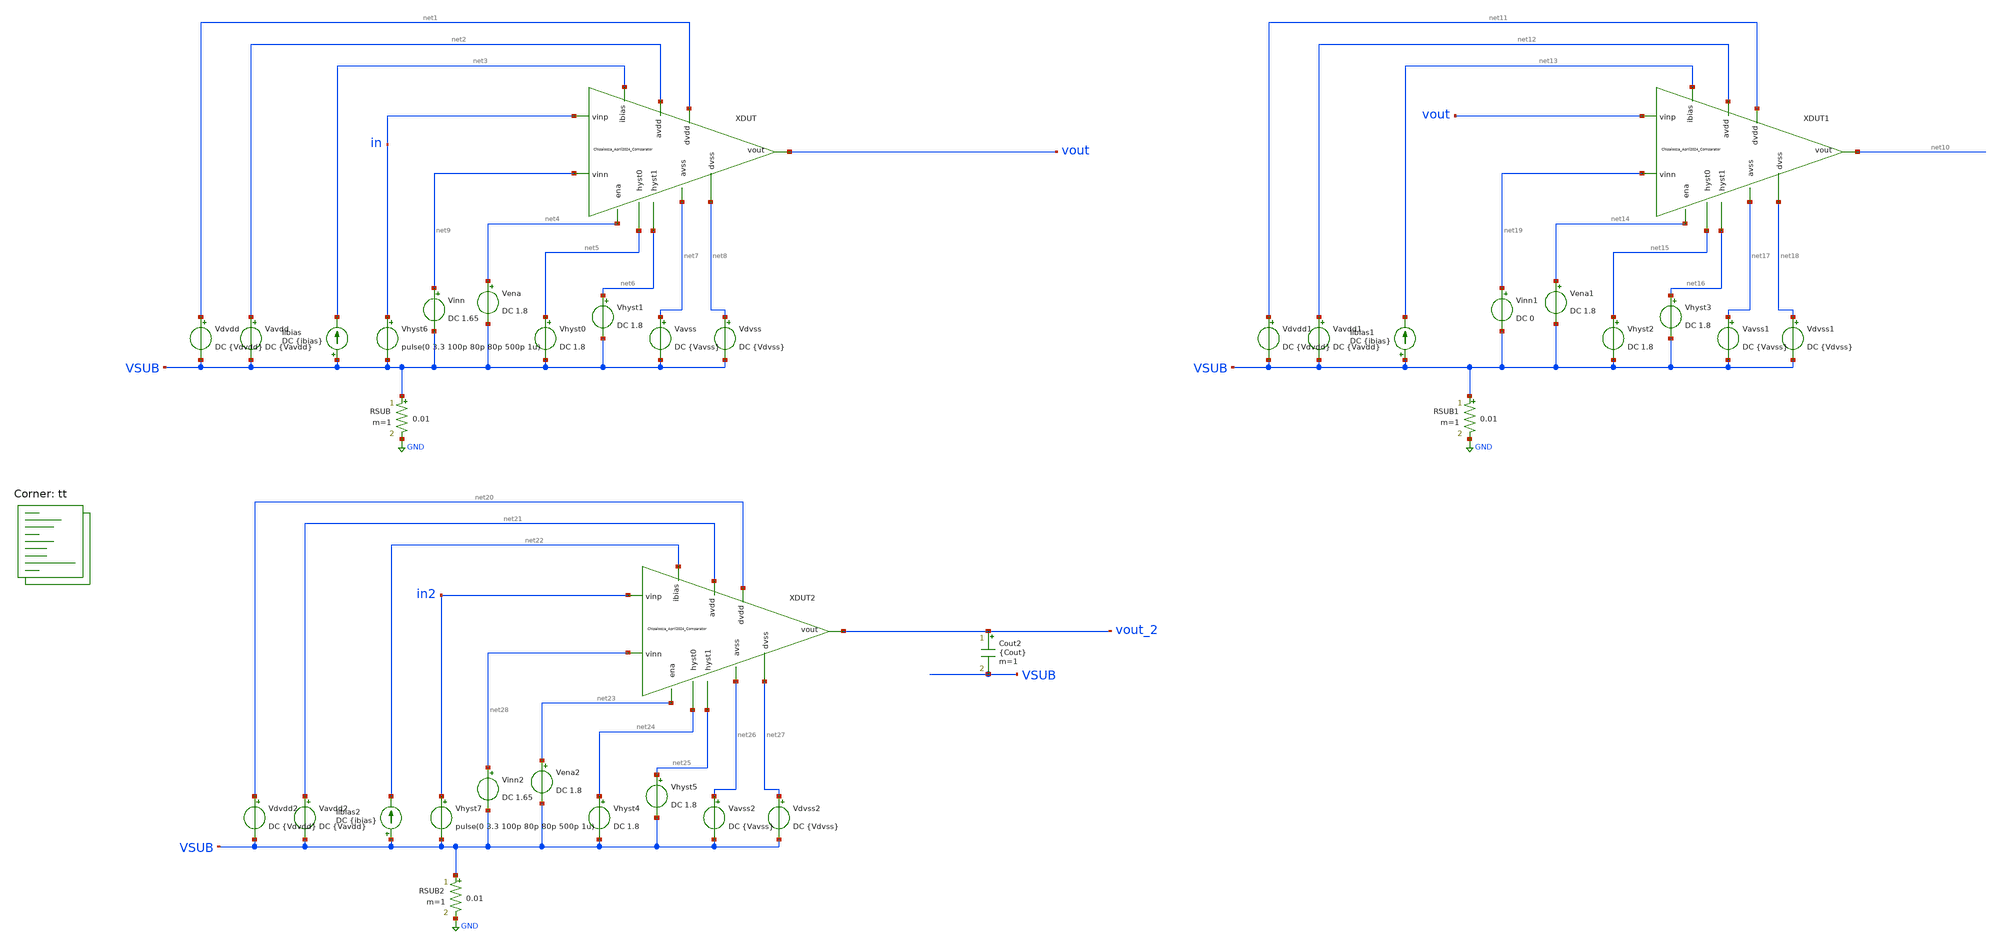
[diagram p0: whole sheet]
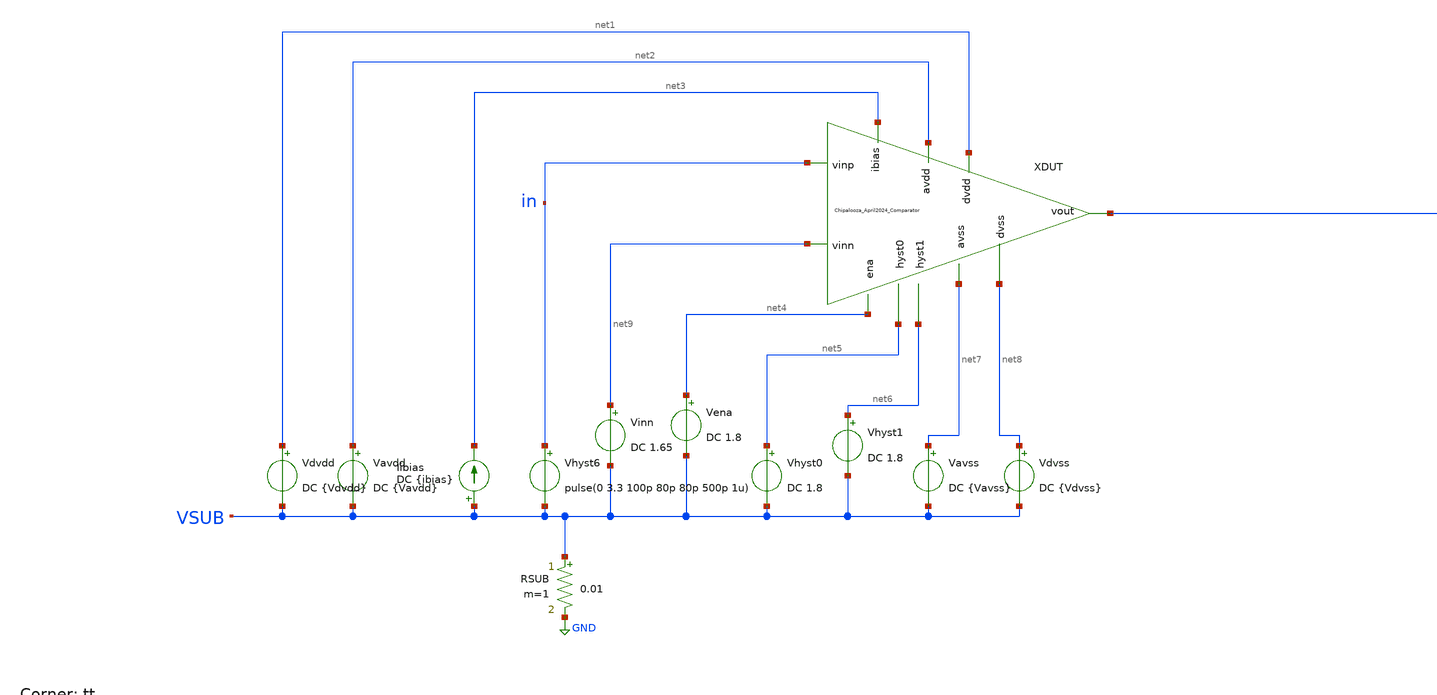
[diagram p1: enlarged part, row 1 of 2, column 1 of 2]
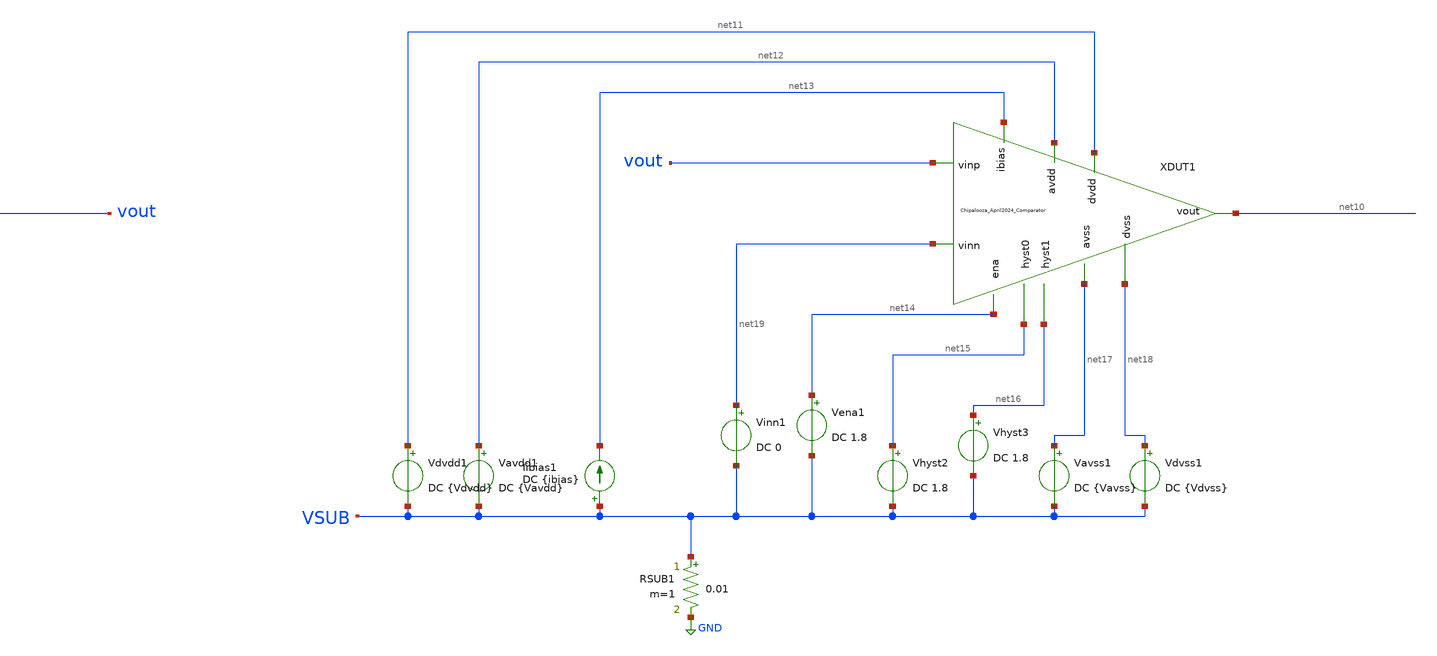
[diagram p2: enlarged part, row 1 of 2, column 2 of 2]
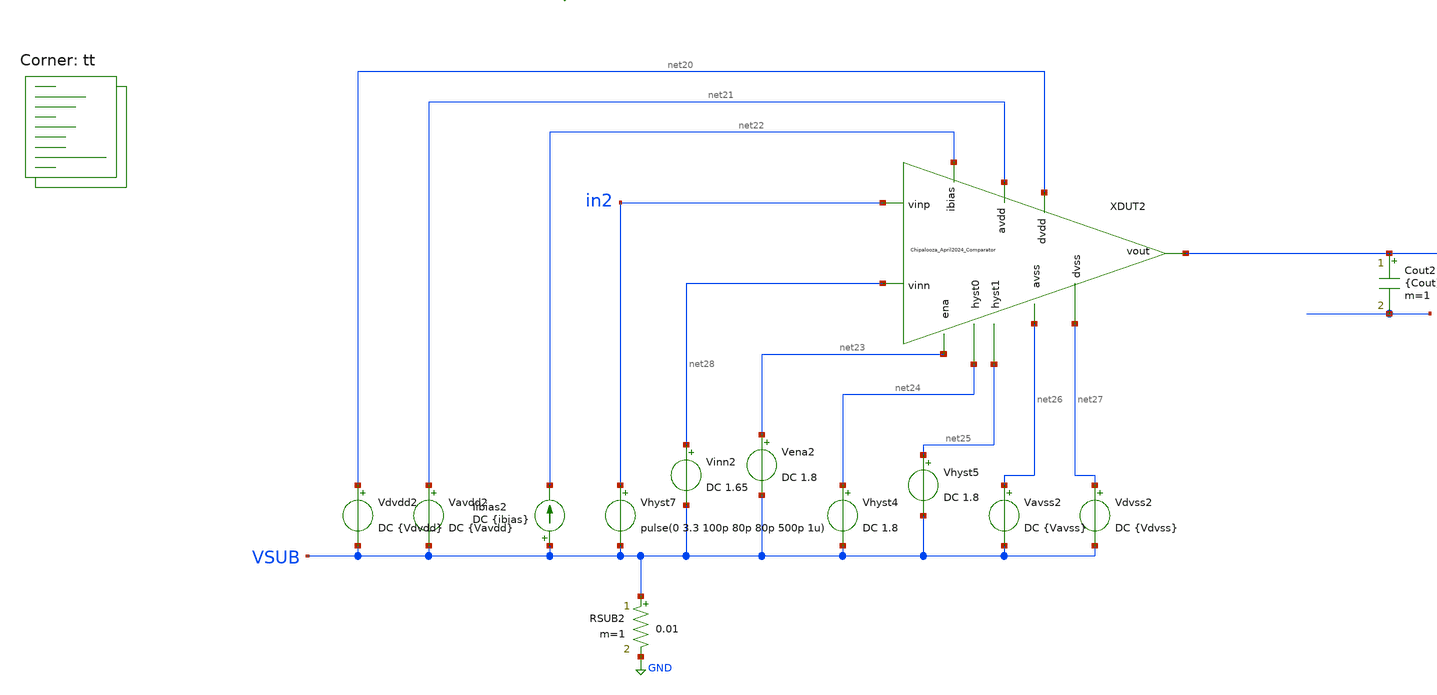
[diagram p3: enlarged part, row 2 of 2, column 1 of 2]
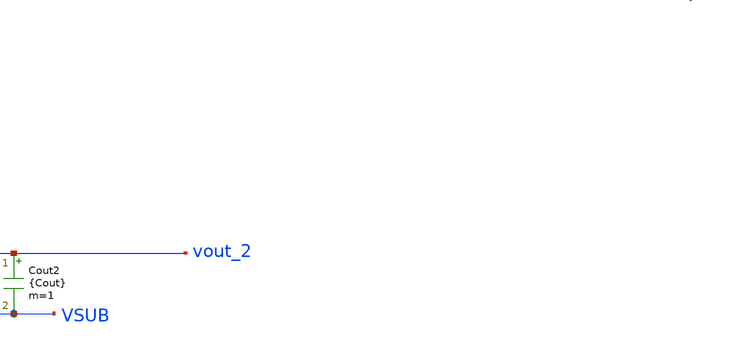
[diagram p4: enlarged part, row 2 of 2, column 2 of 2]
** sch_path: Chipalooza_April2024_Comparator/xschem/TB_inputCapacitance.sch
**.subckt TB_inputCapacitance
Vavdd net2 VSUB DC {Vavdd}
Vdvdd net1 VSUB DC {Vdvdd}
Vena net4 VSUB DC 1.8
Vhyst0 net5 VSUB DC 1.8
Vhyst1 net6 VSUB DC 1.8
Vavss net7 VSUB DC {Vavss}
Vdvss net8 VSUB DC {Vdvss}
RSUB VSUB GND 0.01 m=1
Iibias VSUB net3 DC {ibias}
XDUT net5 net6 net2 in net7 net9 net1 net8 vout net3 net4 Chipalooza_April2024_Comparator
Vinn net9 VSUB DC 1.65
Vavdd1 net12 VSUB DC {Vavdd}
Vdvdd1 net11 VSUB DC {Vdvdd}
Vena1 net14 VSUB DC 1.8
Vhyst2 net15 VSUB DC 1.8
Vhyst3 net16 VSUB DC 1.8
Vavss1 net17 VSUB DC {Vavss}
Vdvss1 net18 VSUB DC {Vdvss}
RSUB1 VSUB GND 0.01 m=1
Iibias1 VSUB net13 DC {ibias}
XDUT1 net15 net16 net12 vout net17 net19 net11 net18 net10 net13 net14
+ Chipalooza_April2024_Comparator
Vavdd2 net21 VSUB DC {Vavdd}
Cout2 vout_2 VSUB {Cout} m=1
Vdvdd2 net20 VSUB DC {Vdvdd}
Vena2 net23 VSUB DC 1.8
Vhyst4 net24 VSUB DC 1.8
Vhyst5 net25 VSUB DC 1.8
Vavss2 net26 VSUB DC {Vavss}
Vdvss2 net27 VSUB DC {Vdvss}
RSUB2 VSUB GND 0.01 m=1
Iibias2 VSUB net22 DC {ibias}
XDUT2 net24 net25 net21 in2 net26 net28 net20 net27 vout_2 net22 net23
+ Chipalooza_April2024_Comparator
Vinn2 net28 VSUB DC 1.65
Vhyst6 in VSUB pulse(0 3.3 100p 80p 80p 500p 1u)
Vhyst7 in2 VSUB pulse(0 3.3 100p 80p 80p 500p 1u)
Vinn1 net19 VSUB DC 0
**** begin user architecture code
.lib $::SKYWATER_MODELS/sky130.lib.spice tt

* this option enables mos model bin
* selection based on W/NF instead of W
*.option wnflag=1
.option savecurrents
.option save all

.control

.param vdvdd=1.8 vavdd=3.3
.param ibias=1u ena=1 Vhyst_0=1 Vhyst_1=1
.param vavss=0 vdvss=0
.param Vcm=1.65
.parm vd=3.3

.param cout=1pF

tran 1ps 1ns
plot v(vout) v(vout_2)


* Measure rising and falling edge (with respect to the output edge) time delays for
* the real copy of the circuit.
*meas TRAN tdr   TRIG v(in) VAL='0.5*vd' FALL=1 TARG v(vout) VAL='0.5*vd' RISE=1
*meas TRAN tdf   TRIG v(in) VAL='0.5*vd' RISE=1 TARG v(vout) VAL='0.5*vd' FALL=1
*meas TRAN tdavg PARAM='(tdr+tdf)/2'

* Measure the same parameters for the model circuit loaded by CLOAD
*meas TRAN tdrc   TRIG v(in2) VAL='0.5*vd' FALL=1 TARG v(vout2) VAL='0.5*vd' RISE=1
*meas TRAN tdfc   TRIG v(in2) VAL='0.5*vd' RISE=1 TARG v(vout2) VAL='0.5*vd' FALL=1
*meas TRAN tdavgc PARAM='(tdrc+tdfc)/2' GOAL=tdavg

*print tdr tdf tdavg tdrc tdfc tdavgc

write TB_inputCapacitance.raw


*quit 0

.endc


**** end user architecture code
**.ends

* expanding   symbol:  Chipalooza_April2024_Comparator.sym # of pins=11
** sym_path: Chipalooza_April2024_Comparator/xschem/Chipalooza_April2024_Comparator.sym
** sch_path: Chipalooza_April2024_Comparator/xschem/Chipalooza_April2024_Comparator.sch
.subckt Chipalooza_April2024_Comparator hyst0 hyst1 avdd vinp avss vinn dvdd dvss vout ibias ena
*.ipin vinp
*.ipin vinn
*.ipin hyst0
*.ipin hyst1
*.ipin avdd
*.ipin avss
*.ipin dvdd
*.ipin dvss
*.opin vout
*.ipin ena
*.ipin ibias
XM29 SumOutBar SumOut dvdd dvdd sky130_fd_pr__pfet_01v8 L=1 W=2 nf=1 ad='int((nf+1)/2) * W/nf * 0.29'
+ as='int((nf+2)/2) * W/nf * 0.29' pd='2*int((nf+1)/2) * (W/nf + 0.29)' ps='2*int((nf+2)/2) * (W/nf + 0.29)'
+ nrd='0.29 / W' nrs='0.29 / W' sa=0 sb=0 sd=0 mult=2 m=2
XM30 SumOutBar SumOut dvssi dvss sky130_fd_pr__nfet_01v8 L=1 W=2 nf=1 ad='int((nf+1)/2) * W/nf * 0.29'
+ as='int((nf+2)/2) * W/nf * 0.29' pd='2*int((nf+1)/2) * (W/nf + 0.29)' ps='2*int((nf+2)/2) * (W/nf + 0.29)'
+ nrd='0.29 / W' nrs='0.29 / W' sa=0 sb=0 sd=0 mult=2 m=2
XM25 net2 hyst_bias0 avss avss sky130_fd_pr__nfet_g5v0d10v5 L=1 W=3 nf=1 ad='int((nf+1)/2) * W/nf * 0.29'
+ as='int((nf+2)/2) * W/nf * 0.29' pd='2*int((nf+1)/2) * (W/nf + 0.29)' ps='2*int((nf+2)/2) * (W/nf + 0.29)'
+ nrd='0.29 / W' nrs='0.29 / W' sa=0 sb=0 sd=0 mult=2 m=2
XM26 hyst_bias0 ibias dvssi dvss sky130_fd_pr__nfet_01v8 L=1 W=3 nf=1 ad='int((1 + 1)/2) * 3 / 1 * 0.29'
+ as='int((1 + 2)/2) * 3 / 1 * 0.29' pd='2*int((1 + 1)/2) * (3 / 1 + 0.29)' ps='2*int((1 + 2)/2) * (3 / 1 + 0.29)'
+ nrd='0.29 / 3 ' nrs='0.29 / 3 ' sa=0 sb=0 sd=0 mult=2 m=2
XM27 ibias ibias dvssi dvss sky130_fd_pr__nfet_01v8 L=1 W=3 nf=1 ad='int((1 + 1)/2) * 3 / 1 * 0.29' as='int((1 + 2)/2) * 3 / 1 * 0.29'
+ pd='2*int((1 + 1)/2) * (3 / 1 + 0.29)' ps='2*int((1 + 2)/2) * (3 / 1 + 0.29)' nrd='0.29 / 3 ' nrs='0.29 / 3 '
+ sa=0 sb=0 sd=0 mult=2 m=2
XM34 hyst_bias1 hyst_bias0 dvdd dvdd sky130_fd_pr__pfet_01v8 L=1 W=3 nf=1 ad='int((nf+1)/2) * W/nf * 0.29'
+ as='int((nf+2)/2) * W/nf * 0.29' pd='2*int((nf+1)/2) * (W/nf + 0.29)' ps='2*int((nf+2)/2) * (W/nf + 0.29)'
+ nrd='0.29 / W' nrs='0.29 / W' sa=0 sb=0 sd=0 mult=2 m=2
XM35 hyst_bias0 hyst_bias0 dvdd dvdd sky130_fd_pr__pfet_01v8 L=1 W=3 nf=1 ad='int((nf+1)/2) * W/nf * 0.29'
+ as='int((nf+2)/2) * W/nf * 0.29' pd='2*int((nf+1)/2) * (W/nf + 0.29)' ps='2*int((nf+2)/2) * (W/nf + 0.29)'
+ nrd='0.29 / W' nrs='0.29 / W' sa=0 sb=0 sd=0 mult=2 m=2
XM36 dvdd hyst_bias1 dvssi dvss sky130_fd_pr__nfet_01v8 L=1 W=3 nf=1 ad='int((1 + 1)/2) * 3 / 1 * 0.29'
+ as='int((1 + 2)/2) * 3 / 1 * 0.29' pd='2*int((1 + 1)/2) * (3 / 1 + 0.29)' ps='2*int((1 + 2)/2) * (3 / 1 + 0.29)'
+ nrd='0.29 / 3 ' nrs='0.29 / 3 ' sa=0 sb=0 sd=0 mult=2 m=2
XM37 hyst_bias1 hyst_bias1 dvssi dvss sky130_fd_pr__nfet_01v8 L=1 W=3 nf=1 ad='int((1 + 1)/2) * 3 / 1 * 0.29'
+ as='int((1 + 2)/2) * 3 / 1 * 0.29' pd='2*int((1 + 1)/2) * (3 / 1 + 0.29)' ps='2*int((1 + 2)/2) * (3 / 1 + 0.29)'
+ nrd='0.29 / 3 ' nrs='0.29 / 3 ' sa=0 sb=0 sd=0 mult=2 m=2
C1 avss 0 2p m=1
XM38 avssi ena avss avss sky130_fd_pr__nfet_g5v0d10v5 L=1 W=16 nf=1 ad='int((nf+1)/2) * W/nf * 0.29'
+ as='int((nf+2)/2) * W/nf * 0.29' pd='2*int((nf+1)/2) * (W/nf + 0.29)' ps='2*int((nf+2)/2) * (W/nf + 0.29)'
+ nrd='0.29 / W' nrs='0.29 / W' sa=0 sb=0 sd=0 mult=2 m=2
XM39 net3 hyst_bias0 avss avss sky130_fd_pr__nfet_g5v0d10v5 L=1 W=8 nf=1 ad='int((nf+1)/2) * W/nf * 0.29'
+ as='int((nf+2)/2) * W/nf * 0.29' pd='2*int((nf+1)/2) * (W/nf + 0.29)' ps='2*int((nf+2)/2) * (W/nf + 0.29)'
+ nrd='0.29 / W' nrs='0.29 / W' sa=0 sb=0 sd=0 mult=4 m=4
XM40 net1 hyst0 net2 avss sky130_fd_pr__nfet_g5v0d10v5 L=1 W=3 nf=1 ad='int((nf+1)/2) * W/nf * 0.29'
+ as='int((nf+2)/2) * W/nf * 0.29' pd='2*int((nf+1)/2) * (W/nf + 0.29)' ps='2*int((nf+2)/2) * (W/nf + 0.29)'
+ nrd='0.29 / W' nrs='0.29 / W' sa=0 sb=0 sd=0 mult=2 m=2
XM41 net1 hyst1 net3 avss sky130_fd_pr__nfet_g5v0d10v5 L=1 W=8 nf=1 ad='int((nf+1)/2) * W/nf * 0.29'
+ as='int((nf+2)/2) * W/nf * 0.29' pd='2*int((nf+1)/2) * (W/nf + 0.29)' ps='2*int((nf+2)/2) * (W/nf + 0.29)'
+ nrd='0.29 / W' nrs='0.29 / W' sa=0 sb=0 sd=0 mult=4 m=4
C2 avss 0 2p m=1
XM13 dvssi ena avss avss sky130_fd_pr__nfet_g5v0d10v5 L=1 W=16 nf=1 ad='int((nf+1)/2) * W/nf * 0.29'
+ as='int((nf+2)/2) * W/nf * 0.29' pd='2*int((nf+1)/2) * (W/nf + 0.29)' ps='2*int((nf+2)/2) * (W/nf + 0.29)'
+ nrd='0.29 / W' nrs='0.29 / W' sa=0 sb=0 sd=0 mult=2 m=2
XM16 vout SumOutBar dvdd dvdd sky130_fd_pr__pfet_01v8 L=1 W=2 nf=1 ad='int((nf+1)/2) * W/nf * 0.29' as='int((nf+2)/2) * W/nf * 0.29'
+ pd='2*int((nf+1)/2) * (W/nf + 0.29)' ps='2*int((nf+2)/2) * (W/nf + 0.29)' nrd='0.29 / W' nrs='0.29 / W'
+ sa=0 sb=0 sd=0 mult=2 m=2
XM18 vout SumOutBar dvssi dvss sky130_fd_pr__nfet_01v8 L=1 W=2 nf=1 ad='int((nf+1)/2) * W/nf * 0.29'
+ as='int((nf+2)/2) * W/nf * 0.29' pd='2*int((nf+1)/2) * (W/nf + 0.29)' ps='2*int((nf+2)/2) * (W/nf + 0.29)'
+ nrd='0.29 / W' nrs='0.29 / W' sa=0 sb=0 sd=0 mult=2 m=2
XM19 net14 SumOutBar net15 dvdd sky130_fd_pr__pfet_01v8 L=1 W=2 nf=1 ad='int((nf+1)/2) * W/nf * 0.29'
+ as='int((nf+2)/2) * W/nf * 0.29' pd='2*int((nf+1)/2) * (W/nf + 0.29)' ps='2*int((nf+2)/2) * (W/nf + 0.29)'
+ nrd='0.29 / W' nrs='0.29 / W' sa=0 sb=0 sd=0 mult=2 m=2
XM24 net1 SumOut N2 dvdd sky130_fd_pr__pfet_01v8 L=1 W=2 nf=1 ad='int((nf+1)/2) * W/nf * 0.29' as='int((nf+2)/2) * W/nf * 0.29'
+ pd='2*int((nf+1)/2) * (W/nf + 0.29)' ps='2*int((nf+2)/2) * (W/nf + 0.29)' nrd='0.29 / W' nrs='0.29 / W'
+ sa=0 sb=0 sd=0 mult=2 m=2
XM4 SourceBias2 SourceBias2 avdd avdd sky130_fd_pr__pfet_g5v0d10v5 L=1 W=2 nf=1 ad='int((nf+1)/2) * W/nf * 0.29'
+ as='int((nf+2)/2) * W/nf * 0.29' pd='2*int((nf+1)/2) * (W/nf + 0.29)' ps='2*int((nf+2)/2) * (W/nf + 0.29)'
+ nrd='0.29 / W' nrs='0.29 / W' sa=0 sb=0 sd=0 mult=2 m=2
XM5 N1 SourceBias2 avdd avdd sky130_fd_pr__pfet_g5v0d10v5 L=1 W=2 nf=1 ad='int((nf+1)/2) * W/nf * 0.29'
+ as='int((nf+2)/2) * W/nf * 0.29' pd='2*int((nf+1)/2) * (W/nf + 0.29)' ps='2*int((nf+2)/2) * (W/nf + 0.29)'
+ nrd='0.29 / W' nrs='0.29 / W' sa=0 sb=0 sd=0 mult=2 m=2
XM6 N2 SourceBias2 avdd avdd sky130_fd_pr__pfet_g5v0d10v5 L=1 W=2 nf=1 ad='int((nf+1)/2) * W/nf * 0.29'
+ as='int((nf+2)/2) * W/nf * 0.29' pd='2*int((nf+1)/2) * (W/nf + 0.29)' ps='2*int((nf+2)/2) * (W/nf + 0.29)'
+ nrd='0.29 / W' nrs='0.29 / W' sa=0 sb=0 sd=0 mult=2 m=2
XM7 SumOut Bias1 N2 avdd sky130_fd_pr__pfet_g5v0d10v5 L=1 W=2 nf=1 ad='int((nf+1)/2) * W/nf * 0.29' as='int((nf+2)/2) * W/nf * 0.29'
+ pd='2*int((nf+1)/2) * (W/nf + 0.29)' ps='2*int((nf+2)/2) * (W/nf + 0.29)' nrd='0.29 / W' nrs='0.29 / W'
+ sa=0 sb=0 sd=0 mult=2 m=2
XM8 Sum Bias1 N1 avdd sky130_fd_pr__pfet_g5v0d10v5 L=1 W=2 nf=1 ad='int((nf+1)/2) * W/nf * 0.29' as='int((nf+2)/2) * W/nf * 0.29'
+ pd='2*int((nf+1)/2) * (W/nf + 0.29)' ps='2*int((nf+2)/2) * (W/nf + 0.29)' nrd='0.29 / W' nrs='0.29 / W'
+ sa=0 sb=0 sd=0 mult=2 m=2
XM9 SumOut Bias2 P2 avss sky130_fd_pr__nfet_g5v0d10v5 L=1 W=2 nf=1 ad='int((nf+1)/2) * W/nf * 0.29' as='int((nf+2)/2) * W/nf * 0.29'
+ pd='2*int((nf+1)/2) * (W/nf + 0.29)' ps='2*int((nf+2)/2) * (W/nf + 0.29)' nrd='0.29 / W' nrs='0.29 / W'
+ sa=0 sb=0 sd=0 mult=2 m=2
XM10 Sum Bias2 P1 avss sky130_fd_pr__nfet_g5v0d10v5 L=1 W=2 nf=1 ad='int((nf+1)/2) * W/nf * 0.29' as='int((nf+2)/2) * W/nf * 0.29'
+ pd='2*int((nf+1)/2) * (W/nf + 0.29)' ps='2*int((nf+2)/2) * (W/nf + 0.29)' nrd='0.29 / W' nrs='0.29 / W'
+ sa=0 sb=0 sd=0 mult=2 m=2
XM11 P2 Sum avss avss sky130_fd_pr__nfet_g5v0d10v5 L=1 W=2 nf=1 ad='int((nf+1)/2) * W/nf * 0.29' as='int((nf+2)/2) * W/nf * 0.29'
+ pd='2*int((nf+1)/2) * (W/nf + 0.29)' ps='2*int((nf+2)/2) * (W/nf + 0.29)' nrd='0.29 / W' nrs='0.29 / W'
+ sa=0 sb=0 sd=0 mult=2 m=2
XM12 P1 Sum avss avss sky130_fd_pr__nfet_g5v0d10v5 L=1 W=2 nf=1 ad='int((nf+1)/2) * W/nf * 0.29' as='int((nf+2)/2) * W/nf * 0.29'
+ pd='2*int((nf+1)/2) * (W/nf + 0.29)' ps='2*int((nf+2)/2) * (W/nf + 0.29)' nrd='0.29 / W' nrs='0.29 / W'
+ sa=0 sb=0 sd=0 mult=2 m=2
XM2 P2 vinn psource_input avdd sky130_fd_pr__pfet_g5v0d10v5 L=1 W=4 nf=1 ad='int((nf+1)/2) * W/nf * 0.29'
+ as='int((nf+2)/2) * W/nf * 0.29' pd='2*int((nf+1)/2) * (W/nf + 0.29)' ps='2*int((nf+2)/2) * (W/nf + 0.29)'
+ nrd='0.29 / W' nrs='0.29 / W' sa=0 sb=0 sd=0 mult=2 m=2
XM3 P1 vinp psource_input avdd sky130_fd_pr__pfet_g5v0d10v5 L=1 W=4 nf=1 ad='int((nf+1)/2) * W/nf * 0.29'
+ as='int((nf+2)/2) * W/nf * 0.29' pd='2*int((nf+1)/2) * (W/nf + 0.29)' ps='2*int((nf+2)/2) * (W/nf + 0.29)'
+ nrd='0.29 / W' nrs='0.29 / W' sa=0 sb=0 sd=0 mult=2 m=2
XM14 psource_input net4 avdd avdd sky130_fd_pr__pfet_g5v0d10v5 L=1 W=12 nf=1 ad='int((nf+1)/2) * W/nf * 0.29'
+ as='int((nf+2)/2) * W/nf * 0.29' pd='2*int((nf+1)/2) * (W/nf + 0.29)' ps='2*int((nf+2)/2) * (W/nf + 0.29)'
+ nrd='0.29 / W' nrs='0.29 / W' sa=0 sb=0 sd=0 mult=4 m=4
XM15 net4 net4 avdd avdd sky130_fd_pr__pfet_g5v0d10v5 L=1 W=8 nf=1 ad='int((nf+1)/2) * W/nf * 0.29' as='int((nf+2)/2) * W/nf * 0.29'
+ pd='2*int((nf+1)/2) * (W/nf + 0.29)' ps='2*int((nf+2)/2) * (W/nf + 0.29)' nrd='0.29 / W' nrs='0.29 / W'
+ sa=0 sb=0 sd=0 mult=2 m=2
XM17 nbias_tail net6 psource_input avdd sky130_fd_pr__pfet_g5v0d10v5 L=1 W=8 nf=1 ad='int((nf+1)/2) * W/nf * 0.29'
+ as='int((nf+2)/2) * W/nf * 0.29' pd='2*int((nf+1)/2) * (W/nf + 0.29)' ps='2*int((nf+2)/2) * (W/nf + 0.29)'
+ nrd='0.29 / W' nrs='0.29 / W' sa=0 sb=0 sd=0 mult=2 m=2
XM20 N1 vinp SourceBias0 avss sky130_fd_pr__nfet_g5v0d10v5 L=4 W=16 nf=1 ad='int((nf+1)/2) * W/nf * 0.29'
+ as='int((nf+2)/2) * W/nf * 0.29' pd='2*int((nf+1)/2) * (W/nf + 0.29)' ps='2*int((nf+2)/2) * (W/nf + 0.29)'
+ nrd='0.29 / W' nrs='0.29 / W' sa=0 sb=0 sd=0 mult=2 m=2
XM21 N2 vinn SourceBias0 avss sky130_fd_pr__nfet_g5v0d10v5 L=4 W=16 nf=1 ad='int((nf+1)/2) * W/nf * 0.29'
+ as='int((nf+2)/2) * W/nf * 0.29' pd='2*int((nf+1)/2) * (W/nf + 0.29)' ps='2*int((nf+2)/2) * (W/nf + 0.29)'
+ nrd='0.29 / W' nrs='0.29 / W' sa=0 sb=0 sd=0 mult=2 m=2
XM22 SourceBias0 nbias_tail avssi avss sky130_fd_pr__nfet_g5v0d10v5 L=1 W=12 nf=1 ad='int((nf+1)/2) * W/nf * 0.29'
+ as='int((nf+2)/2) * W/nf * 0.29' pd='2*int((nf+1)/2) * (W/nf + 0.29)' ps='2*int((nf+2)/2) * (W/nf + 0.29)'
+ nrd='0.29 / W' nrs='0.29 / W' sa=0 sb=0 sd=0 mult=4 m=4
XM23 nbias_tail nbias_tail avssi avss sky130_fd_pr__nfet_g5v0d10v5 L=1 W=12 nf=1 ad='int((nf+1)/2) * W/nf * 0.29'
+ as='int((nf+2)/2) * W/nf * 0.29' pd='2*int((nf+1)/2) * (W/nf + 0.29)' ps='2*int((nf+2)/2) * (W/nf + 0.29)'
+ nrd='0.29 / W' nrs='0.29 / W' sa=0 sb=0 sd=0 mult=2 m=2
XM28 net4 Bias5 SourceBias0 avss sky130_fd_pr__nfet_g5v0d10v5 L=1 W=4 nf=1 ad='int((nf+1)/2) * W/nf * 0.29'
+ as='int((nf+2)/2) * W/nf * 0.29' pd='2*int((nf+1)/2) * (W/nf + 0.29)' ps='2*int((nf+2)/2) * (W/nf + 0.29)'
+ nrd='0.29 / W' nrs='0.29 / W' sa=0 sb=0 sd=0 mult=2 m=2
XM31 SourceBias0 net5 avssi avss sky130_fd_pr__nfet_g5v0d10v5 L=4 W=16 nf=1 ad='int((nf+1)/2) * W/nf * 0.29'
+ as='int((nf+2)/2) * W/nf * 0.29' pd='2*int((nf+1)/2) * (W/nf + 0.29)' ps='2*int((nf+2)/2) * (W/nf + 0.29)'
+ nrd='0.29 / W' nrs='0.29 / W' sa=0 sb=0 sd=0 mult=2 m=2
XM44 net5 net5 avssi avss sky130_fd_pr__nfet_g5v0d10v5 L=4 W=16 nf=1 ad='int((nf+1)/2) * W/nf * 0.29'
+ as='int((nf+2)/2) * W/nf * 0.29' pd='2*int((nf+1)/2) * (W/nf + 0.29)' ps='2*int((nf+2)/2) * (W/nf + 0.29)'
+ nrd='0.29 / W' nrs='0.29 / W' sa=0 sb=0 sd=0 mult=2 m=2
XM45 SourceBias1 net5 avssi avss sky130_fd_pr__nfet_g5v0d10v5 L=4 W=16 nf=1 ad='int((nf+1)/2) * W/nf * 0.29'
+ as='int((nf+2)/2) * W/nf * 0.29' pd='2*int((nf+1)/2) * (W/nf + 0.29)' ps='2*int((nf+2)/2) * (W/nf + 0.29)'
+ nrd='0.29 / W' nrs='0.29 / W' sa=0 sb=0 sd=0 mult=2 m=2
XM46 SourceBias1 SourceBias1 avdd avdd sky130_fd_pr__pfet_g5v0d10v5 L=1 W=12 nf=1 ad='int((nf+1)/2) * W/nf * 0.29'
+ as='int((nf+2)/2) * W/nf * 0.29' pd='2*int((nf+1)/2) * (W/nf + 0.29)' ps='2*int((nf+2)/2) * (W/nf + 0.29)'
+ nrd='0.29 / W' nrs='0.29 / W' sa=0 sb=0 sd=0 mult=4 m=4
XM47 psource_input SourceBias1 avdd avdd sky130_fd_pr__pfet_g5v0d10v5 L=1 W=12 nf=1 ad='int((nf+1)/2) * W/nf * 0.29'
+ as='int((nf+2)/2) * W/nf * 0.29' pd='2*int((nf+1)/2) * (W/nf + 0.29)' ps='2*int((nf+2)/2) * (W/nf + 0.29)'
+ nrd='0.29 / W' nrs='0.29 / W' sa=0 sb=0 sd=0 mult=4 m=4
XM48 SourceBias2 net5 avssi avss sky130_fd_pr__nfet_g5v0d10v5 L=4 W=16 nf=1 ad='int((nf+1)/2) * W/nf * 0.29'
+ as='int((nf+2)/2) * W/nf * 0.29' pd='2*int((nf+1)/2) * (W/nf + 0.29)' ps='2*int((nf+2)/2) * (W/nf + 0.29)'
+ nrd='0.29 / W' nrs='0.29 / W' sa=0 sb=0 sd=0 mult=4 m=4
XM63 net6 net6 avdd avdd sky130_fd_pr__pfet_g5v0d10v5 L=5 W=3 nf=1 ad='int((nf+1)/2) * W/nf * 0.29' as='int((nf+2)/2) * W/nf * 0.29'
+ pd='2*int((nf+1)/2) * (W/nf + 0.29)' ps='2*int((nf+2)/2) * (W/nf + 0.29)' nrd='0.29 / W' nrs='0.29 / W'
+ sa=0 sb=0 sd=0 mult=1 m=1
XM62 avdd Bias4 SourceBias3 avss sky130_fd_pr__nfet_g5v0d10v5 L=1 W=4 nf=1 ad='int((nf+1)/2) * W/nf * 0.29'
+ as='int((nf+2)/2) * W/nf * 0.29' pd='2*int((nf+1)/2) * (W/nf + 0.29)' ps='2*int((nf+2)/2) * (W/nf + 0.29)'
+ nrd='0.29 / W' nrs='0.29 / W' sa=0 sb=0 sd=0 mult=2 m=2
XM64 net6 Bias4 SourceBias3 avss sky130_fd_pr__nfet_g5v0d10v5 L=1 W=4 nf=1 ad='int((nf+1)/2) * W/nf * 0.29'
+ as='int((nf+2)/2) * W/nf * 0.29' pd='2*int((nf+1)/2) * (W/nf + 0.29)' ps='2*int((nf+2)/2) * (W/nf + 0.29)'
+ nrd='0.29 / W' nrs='0.29 / W' sa=0 sb=0 sd=0 mult=2 m=2
XM65 SourceBias3 net5 avssi avss sky130_fd_pr__nfet_g5v0d10v5 L=4 W=16 nf=1 ad='int((nf+1)/2) * W/nf * 0.29'
+ as='int((nf+2)/2) * W/nf * 0.29' pd='2*int((nf+1)/2) * (W/nf + 0.29)' ps='2*int((nf+2)/2) * (W/nf + 0.29)'
+ nrd='0.29 / W' nrs='0.29 / W' sa=0 sb=0 sd=0 mult=4 m=4
XM76 Bias1 net5 avssi avss sky130_fd_pr__nfet_g5v0d10v5 L=4 W=16 nf=1 ad='int((nf+1)/2) * W/nf * 0.29'
+ as='int((nf+2)/2) * W/nf * 0.29' pd='2*int((nf+1)/2) * (W/nf + 0.29)' ps='2*int((nf+2)/2) * (W/nf + 0.29)'
+ nrd='0.29 / W' nrs='0.29 / W' sa=0 sb=0 sd=0 mult=4 m=4
XM77 SourceBias5 net5 avssi avss sky130_fd_pr__nfet_g5v0d10v5 L=4 W=16 nf=1 ad='int((nf+1)/2) * W/nf * 0.29'
+ as='int((nf+2)/2) * W/nf * 0.29' pd='2*int((nf+1)/2) * (W/nf + 0.29)' ps='2*int((nf+2)/2) * (W/nf + 0.29)'
+ nrd='0.29 / W' nrs='0.29 / W' sa=0 sb=0 sd=0 mult=4 m=4
XM78 SourceBias6 net5 avssi avss sky130_fd_pr__nfet_g5v0d10v5 L=4 W=16 nf=1 ad='int((nf+1)/2) * W/nf * 0.29'
+ as='int((nf+2)/2) * W/nf * 0.29' pd='2*int((nf+1)/2) * (W/nf + 0.29)' ps='2*int((nf+2)/2) * (W/nf + 0.29)'
+ nrd='0.29 / W' nrs='0.29 / W' sa=0 sb=0 sd=0 mult=4 m=4
XM79 SourceBias7 net5 avssi avss sky130_fd_pr__nfet_g5v0d10v5 L=4 W=16 nf=1 ad='int((nf+1)/2) * W/nf * 0.29'
+ as='int((nf+2)/2) * W/nf * 0.29' pd='2*int((nf+1)/2) * (W/nf + 0.29)' ps='2*int((nf+2)/2) * (W/nf + 0.29)'
+ nrd='0.29 / W' nrs='0.29 / W' sa=0 sb=0 sd=0 mult=4 m=4
XM81 Bias5 net5 avssi avss sky130_fd_pr__nfet_g5v0d10v5 L=4 W=16 nf=1 ad='int((nf+1)/2) * W/nf * 0.29'
+ as='int((nf+2)/2) * W/nf * 0.29' pd='2*int((nf+1)/2) * (W/nf + 0.29)' ps='2*int((nf+2)/2) * (W/nf + 0.29)'
+ nrd='0.29 / W' nrs='0.29 / W' sa=0 sb=0 sd=0 mult=4 m=4
XM82 Bias4 net5 avssi avss sky130_fd_pr__nfet_g5v0d10v5 L=4 W=16 nf=1 ad='int((nf+1)/2) * W/nf * 0.29'
+ as='int((nf+2)/2) * W/nf * 0.29' pd='2*int((nf+1)/2) * (W/nf + 0.29)' ps='2*int((nf+2)/2) * (W/nf + 0.29)'
+ nrd='0.29 / W' nrs='0.29 / W' sa=0 sb=0 sd=0 mult=4 m=4
XM83 SourceBias10 net5 avssi avss sky130_fd_pr__nfet_g5v0d10v5 L=4 W=16 nf=1 ad='int((nf+1)/2) * W/nf * 0.29'
+ as='int((nf+2)/2) * W/nf * 0.29' pd='2*int((nf+1)/2) * (W/nf + 0.29)' ps='2*int((nf+2)/2) * (W/nf + 0.29)'
+ nrd='0.29 / W' nrs='0.29 / W' sa=0 sb=0 sd=0 mult=4 m=4
XM1 ibias ibias avssi avss sky130_fd_pr__nfet_g5v0d10v5 L=4 W=16 nf=1 ad='int((nf+1)/2) * W/nf * 0.29'
+ as='int((nf+2)/2) * W/nf * 0.29' pd='2*int((nf+1)/2) * (W/nf + 0.29)' ps='2*int((nf+2)/2) * (W/nf + 0.29)'
+ nrd='0.29 / W' nrs='0.29 / W' sa=0 sb=0 sd=0 mult=2 m=2
XM32 net7 ibias avssi avss sky130_fd_pr__nfet_g5v0d10v5 L=4 W=16 nf=1 ad='int((nf+1)/2) * W/nf * 0.29'
+ as='int((nf+2)/2) * W/nf * 0.29' pd='2*int((nf+1)/2) * (W/nf + 0.29)' ps='2*int((nf+2)/2) * (W/nf + 0.29)'
+ nrd='0.29 / W' nrs='0.29 / W' sa=0 sb=0 sd=0 mult=2 m=2
XM33 net7 net7 avdd avdd sky130_fd_pr__pfet_g5v0d10v5 L=1 W=8 nf=1 ad='int((nf+1)/2) * W/nf * 0.29' as='int((nf+2)/2) * W/nf * 0.29'
+ pd='2*int((nf+1)/2) * (W/nf + 0.29)' ps='2*int((nf+2)/2) * (W/nf + 0.29)' nrd='0.29 / W' nrs='0.29 / W'
+ sa=0 sb=0 sd=0 mult=2 m=2
XM42 net5 net7 avdd avdd sky130_fd_pr__pfet_g5v0d10v5 L=1 W=8 nf=1 ad='int((nf+1)/2) * W/nf * 0.29' as='int((nf+2)/2) * W/nf * 0.29'
+ pd='2*int((nf+1)/2) * (W/nf + 0.29)' ps='2*int((nf+2)/2) * (W/nf + 0.29)' nrd='0.29 / W' nrs='0.29 / W'
+ sa=0 sb=0 sd=0 mult=2 m=2
XM54 M55Source M55Drain avss avss sky130_fd_pr__nfet_g5v0d10v5 L=1.5 W=6 nf=1 ad='int((nf+1)/2) * W/nf * 0.29'
+ as='int((nf+2)/2) * W/nf * 0.29' pd='2*int((nf+1)/2) * (W/nf + 0.29)' ps='2*int((nf+2)/2) * (W/nf + 0.29)'
+ nrd='0.29 / W' nrs='0.29 / W' sa=0 sb=0 sd=0 mult=2 m=2
XM55 M55Drain Bias2 M55Source avss sky130_fd_pr__nfet_g5v0d10v5 L=1 W=9 nf=1 ad='int((nf+1)/2) * W/nf * 0.29'
+ as='int((nf+2)/2) * W/nf * 0.29' pd='2*int((nf+1)/2) * (W/nf + 0.29)' ps='2*int((nf+2)/2) * (W/nf + 0.29)'
+ nrd='0.29 / W' nrs='0.29 / W' sa=0 sb=0 sd=0 mult=2 m=2
XM56 Bias2 Bias2 avss avss sky130_fd_pr__nfet_g5v0d10v5 L=2 W=0.5 nf=1 ad='int((nf+1)/2) * W/nf * 0.29'
+ as='int((nf+2)/2) * W/nf * 0.29' pd='2*int((nf+1)/2) * (W/nf + 0.29)' ps='2*int((nf+2)/2) * (W/nf + 0.29)'
+ nrd='0.29 / W' nrs='0.29 / W' sa=0 sb=0 sd=0 mult=1 m=1
XM51 net8 net9 avdd avdd sky130_fd_pr__pfet_g5v0d10v5 L=2 W=20 nf=1 ad='int((nf+1)/2) * W/nf * 0.29'
+ as='int((nf+2)/2) * W/nf * 0.29' pd='2*int((nf+1)/2) * (W/nf + 0.29)' ps='2*int((nf+2)/2) * (W/nf + 0.29)'
+ nrd='0.29 / W' nrs='0.29 / W' sa=0 sb=0 sd=0 mult=2 m=2
XM49 net9 net9 avdd avdd sky130_fd_pr__pfet_g5v0d10v5 L=2 W=10 nf=1 ad='int((nf+1)/2) * W/nf * 0.29'
+ as='int((nf+2)/2) * W/nf * 0.29' pd='2*int((nf+1)/2) * (W/nf + 0.29)' ps='2*int((nf+2)/2) * (W/nf + 0.29)'
+ nrd='0.29 / W' nrs='0.29 / W' sa=0 sb=0 sd=0 mult=2 m=2
XM50 SourceBias4 SourceBias4 net9 avdd sky130_fd_pr__pfet_g5v0d10v5 L=1 W=10 nf=1 ad='int((nf+1)/2) * W/nf * 0.29'
+ as='int((nf+2)/2) * W/nf * 0.29' pd='2*int((nf+1)/2) * (W/nf + 0.29)' ps='2*int((nf+2)/2) * (W/nf + 0.29)'
+ nrd='0.29 / W' nrs='0.29 / W' sa=0 sb=0 sd=0 mult=2 m=2
XM52 avss SourceBias4 net8 avdd sky130_fd_pr__pfet_g5v0d10v5 L=1 W=1 nf=1 ad='int((nf+1)/2) * W/nf * 0.29'
+ as='int((nf+2)/2) * W/nf * 0.29' pd='2*int((nf+1)/2) * (W/nf + 0.29)' ps='2*int((nf+2)/2) * (W/nf + 0.29)'
+ nrd='0.29 / W' nrs='0.29 / W' sa=0 sb=0 sd=0 mult=2 m=2
XM53 Bias1 Bias1 net8 avdd sky130_fd_pr__pfet_g5v0d10v5 L=1 W=10 nf=1 ad='int((nf+1)/2) * W/nf * 0.29'
+ as='int((nf+2)/2) * W/nf * 0.29' pd='2*int((nf+1)/2) * (W/nf + 0.29)' ps='2*int((nf+2)/2) * (W/nf + 0.29)'
+ nrd='0.29 / W' nrs='0.29 / W' sa=0 sb=0 sd=0 mult=2 m=2
XM57 net10 net11 avdd avdd sky130_fd_pr__pfet_g5v0d10v5 L=2 W=20 nf=1 ad='int((nf+1)/2) * W/nf * 0.29'
+ as='int((nf+2)/2) * W/nf * 0.29' pd='2*int((nf+1)/2) * (W/nf + 0.29)' ps='2*int((nf+2)/2) * (W/nf + 0.29)'
+ nrd='0.29 / W' nrs='0.29 / W' sa=0 sb=0 sd=0 mult=2 m=2
XM58 net11 net11 avdd avdd sky130_fd_pr__pfet_g5v0d10v5 L=2 W=10 nf=1 ad='int((nf+1)/2) * W/nf * 0.29'
+ as='int((nf+2)/2) * W/nf * 0.29' pd='2*int((nf+1)/2) * (W/nf + 0.29)' ps='2*int((nf+2)/2) * (W/nf + 0.29)'
+ nrd='0.29 / W' nrs='0.29 / W' sa=0 sb=0 sd=0 mult=2 m=2
XM59 SourceBias10 SourceBias10 net11 avdd sky130_fd_pr__pfet_g5v0d10v5 L=1 W=10 nf=1 ad='int((nf+1)/2) * W/nf * 0.29'
+ as='int((nf+2)/2) * W/nf * 0.29' pd='2*int((nf+1)/2) * (W/nf + 0.29)' ps='2*int((nf+2)/2) * (W/nf + 0.29)'
+ nrd='0.29 / W' nrs='0.29 / W' sa=0 sb=0 sd=0 mult=2 m=2
XM60 avss SourceBias10 net10 avdd sky130_fd_pr__pfet_g5v0d10v5 L=1 W=1 nf=1 ad='int((nf+1)/2) * W/nf * 0.29'
+ as='int((nf+2)/2) * W/nf * 0.29' pd='2*int((nf+1)/2) * (W/nf + 0.29)' ps='2*int((nf+2)/2) * (W/nf + 0.29)'
+ nrd='0.29 / W' nrs='0.29 / W' sa=0 sb=0 sd=0 mult=2 m=2
XM61 Bias4 Bias4 net10 avdd sky130_fd_pr__pfet_g5v0d10v5 L=1 W=5 nf=1 ad='int((nf+1)/2) * W/nf * 0.29'
+ as='int((nf+2)/2) * W/nf * 0.29' pd='2*int((nf+1)/2) * (W/nf + 0.29)' ps='2*int((nf+2)/2) * (W/nf + 0.29)'
+ nrd='0.29 / W' nrs='0.29 / W' sa=0 sb=0 sd=0 mult=2 m=2
XM66 net12 net13 avdd avdd sky130_fd_pr__pfet_g5v0d10v5 L=2 W=20 nf=1 ad='int((nf+1)/2) * W/nf * 0.29'
+ as='int((nf+2)/2) * W/nf * 0.29' pd='2*int((nf+1)/2) * (W/nf + 0.29)' ps='2*int((nf+2)/2) * (W/nf + 0.29)'
+ nrd='0.29 / W' nrs='0.29 / W' sa=0 sb=0 sd=0 mult=2 m=2
XM67 net13 net13 avdd avdd sky130_fd_pr__pfet_g5v0d10v5 L=2 W=20 nf=1 ad='int((nf+1)/2) * W/nf * 0.29'
+ as='int((nf+2)/2) * W/nf * 0.29' pd='2*int((nf+1)/2) * (W/nf + 0.29)' ps='2*int((nf+2)/2) * (W/nf + 0.29)'
+ nrd='0.29 / W' nrs='0.29 / W' sa=0 sb=0 sd=0 mult=2 m=2
XM68 SourceBias7 SourceBias7 net13 avdd sky130_fd_pr__pfet_g5v0d10v5 L=1 W=10 nf=1 ad='int((nf+1)/2) * W/nf * 0.29'
+ as='int((nf+2)/2) * W/nf * 0.29' pd='2*int((nf+1)/2) * (W/nf + 0.29)' ps='2*int((nf+2)/2) * (W/nf + 0.29)'
+ nrd='0.29 / W' nrs='0.29 / W' sa=0 sb=0 sd=0 mult=2 m=2
XM69 avss SourceBias7 net12 avdd sky130_fd_pr__pfet_g5v0d10v5 L=1 W=1 nf=1 ad='int((nf+1)/2) * W/nf * 0.29'
+ as='int((nf+2)/2) * W/nf * 0.29' pd='2*int((nf+1)/2) * (W/nf + 0.29)' ps='2*int((nf+2)/2) * (W/nf + 0.29)'
+ nrd='0.29 / W' nrs='0.29 / W' sa=0 sb=0 sd=0 mult=2 m=2
XM70 Bias5 Bias5 net12 avdd sky130_fd_pr__pfet_g5v0d10v5 L=1 W=5 nf=1 ad='int((nf+1)/2) * W/nf * 0.29'
+ as='int((nf+2)/2) * W/nf * 0.29' pd='2*int((nf+1)/2) * (W/nf + 0.29)' ps='2*int((nf+2)/2) * (W/nf + 0.29)'
+ nrd='0.29 / W' nrs='0.29 / W' sa=0 sb=0 sd=0 mult=2 m=2
XM72 SourceBias5 SourceBias5 avdd avdd sky130_fd_pr__pfet_g5v0d10v5 L=1 W=12 nf=1 ad='int((nf+1)/2) * W/nf * 0.29'
+ as='int((nf+2)/2) * W/nf * 0.29' pd='2*int((nf+1)/2) * (W/nf + 0.29)' ps='2*int((nf+2)/2) * (W/nf + 0.29)'
+ nrd='0.29 / W' nrs='0.29 / W' sa=0 sb=0 sd=0 mult=4 m=4
XM73 M55Drain SourceBias5 avdd avdd sky130_fd_pr__pfet_g5v0d10v5 L=1 W=12 nf=1 ad='int((nf+1)/2) * W/nf * 0.29'
+ as='int((nf+2)/2) * W/nf * 0.29' pd='2*int((nf+1)/2) * (W/nf + 0.29)' ps='2*int((nf+2)/2) * (W/nf + 0.29)'
+ nrd='0.29 / W' nrs='0.29 / W' sa=0 sb=0 sd=0 mult=4 m=4
XM74 SourceBias6 SourceBias6 avdd avdd sky130_fd_pr__pfet_g5v0d10v5 L=1 W=12 nf=1 ad='int((nf+1)/2) * W/nf * 0.29'
+ as='int((nf+2)/2) * W/nf * 0.29' pd='2*int((nf+1)/2) * (W/nf + 0.29)' ps='2*int((nf+2)/2) * (W/nf + 0.29)'
+ nrd='0.29 / W' nrs='0.29 / W' sa=0 sb=0 sd=0 mult=4 m=4
XM75 Bias2 SourceBias6 avdd avdd sky130_fd_pr__pfet_g5v0d10v5 L=1 W=12 nf=1 ad='int((nf+1)/2) * W/nf * 0.29'
+ as='int((nf+2)/2) * W/nf * 0.29' pd='2*int((nf+1)/2) * (W/nf + 0.29)' ps='2*int((nf+2)/2) * (W/nf + 0.29)'
+ nrd='0.29 / W' nrs='0.29 / W' sa=0 sb=0 sd=0 mult=4 m=4
.ends

.GLOBAL GND
.end
